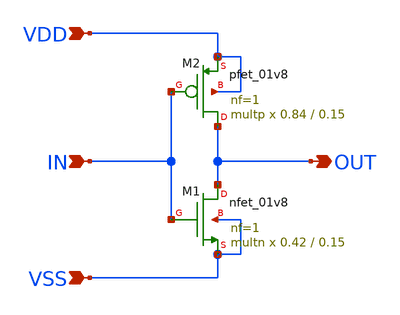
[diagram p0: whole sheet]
** sch_path: module/cdac/var_mult_inv.sch
**.subckt var_mult_inv IN VDD VSS OUT
*.ipin IN
*.ipin VDD
*.ipin VSS
*.opin OUT
XM1 OUT IN VSS VSS sky130_fd_pr__nfet_01v8 L=0.15 W=0.42 nf=1 ad='int((nf+1)/2) * W/nf * 0.29' as='int((nf+2)/2) * W/nf * 0.29'
+ pd='2*int((nf+1)/2) * (W/nf + 0.29)' ps='2*int((nf+2)/2) * (W/nf + 0.29)' nrd='0.29 / W' nrs='0.29 / W'
+ sa=0 sb=0 sd=0 mult=multn m=multn
XM2 OUT IN VDD VDD sky130_fd_pr__pfet_01v8 L=0.15 W=0.84 nf=1 ad='int((nf+1)/2) * W/nf * 0.29' as='int((nf+2)/2) * W/nf * 0.29'
+ pd='2*int((nf+1)/2) * (W/nf + 0.29)' ps='2*int((nf+2)/2) * (W/nf + 0.29)' nrd='0.29 / W' nrs='0.29 / W'
+ sa=0 sb=0 sd=0 mult=multp m=multp
**.ends
.end
